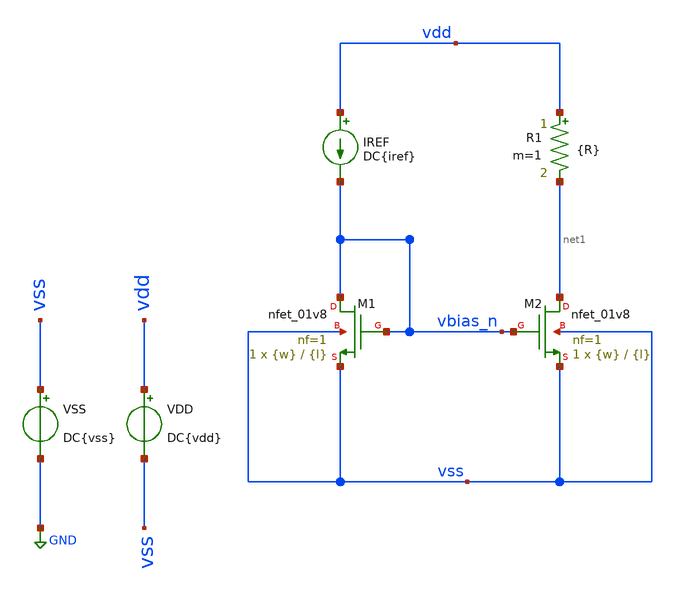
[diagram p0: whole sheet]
** sch_path: TP2/tp2_1.sch
**.subckt tp2_1
XM1 vbias_n vbias_n vss vss sky130_fd_pr__nfet_01v8 L={l} W={w} nf=1 ad='int((nf+1)/2) * W/nf * 0.29'
+ as='int((nf+2)/2) * W/nf * 0.29' pd='2*int((nf+1)/2) * (W/nf + 0.29)' ps='2*int((nf+2)/2) * (W/nf + 0.29)'
+ nrd='0.29 / W' nrs='0.29 / W' sa=0 sb=0 sd=0 mult=1 m=1
XM2 net1 vbias_n vss vss sky130_fd_pr__nfet_01v8 L={l} W={w} nf=1 ad='int((nf+1)/2) * W/nf * 0.29' as='int((nf+2)/2) * W/nf * 0.29'
+ pd='2*int((nf+1)/2) * (W/nf + 0.29)' ps='2*int((nf+2)/2) * (W/nf + 0.29)' nrd='0.29 / W' nrs='0.29 / W'
+ sa=0 sb=0 sd=0 mult=1 m=1
R1 vdd net1 {R} m=1
IREF vdd vbias_n DC{iref}
VSS vss GND DC{vss}
VDD vdd vss DC{vdd}
**** begin user architecture code



* Parameters
.param vdd = 1.8
.param vss = 0.0
.param iref = 200u
.param w = 4.2
.param l = 0.15
.param R = 4.5k
.options TEMPS = 27.0

* Models
.lib ~/skywater/skywater-pdk/libraries/sky130_fd_pr_ngspice/latest/models/corners/sky130.lib TT

* Data to save
.save all  @M.XM1.msky130_fd_pr__nfet_01v8[id]  @M.XM1.msky130_fd_pr__nfet_01v8[vth]  @M.XM1.msky130_fd_pr__nfet_01v8[vdsat]  @M.XM1.msky130_fd_pr__nfet_01v8[gm]  @M.XM1.msky130_fd_pr__nfet_01v8[vds]  @M.XM1.msky130_fd_pr__nfet_01v8[vgs]  @M.XM1.msky130_fd_pr__nfet_01v8[w]  @M.XM2.msky130_fd_pr__nfet_01v8[id]  @M.XM2.msky130_fd_pr__nfet_01v8[gm]  @M.XM2.msky130_fd_pr__nfet_01v8[vds]  @M.XM2.msky130_fd_pr__nfet_01v8[vgs]  @M.XM2.msky130_fd_pr__nfet_01v8[w]

* Simulation
.control
  *let wi = 1.5
  *let wf = 4.5
  *let wstep = 0.15

  *dowhile wi <= wf
    *print @M.XM1.msky130_fd_pr__nfet_01v8[w]
    *alter @M.XM1.msky130_fd_pr__nfet_01v8[w] = wi
    *alter @M.XM2.msky130_fd_pr__nfet_01v8[w] = wi
    *let wi = wi + wstep
    *op
    *print @M.XM1.msky130_fd_pr__nfet_01v8[w]
    *print @M.XM1.msky130_fd_pr__nfet_01v8[id]
    *print @M.XM1.msky130_fd_pr__nfet_01v8[vds]
    *print @M.XM1.msky130_fd_pr__nfet_01v8[vgs]
    *print @M.XM2.msky130_fd_pr__nfet_01v8[w]
    *print @M.XM2.msky130_fd_pr__nfet_01v8[id]
    *print @M.XM2.msky130_fd_pr__nfet_01v8[vds]
    *print @M.XM2.msky130_fd_pr__nfet_01v8[vgs]
    *save all
  *end
  *write tp2_1.raw


  unset filetype
  op
  save all
  write tp2_1.raw

.endc

.end


**** end user architecture code
**.ends
.GLOBAL GND
.end
